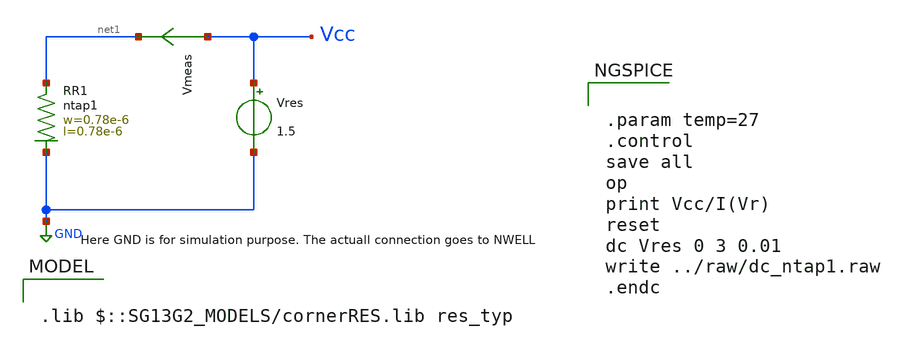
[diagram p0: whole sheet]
** sch_path: ihp-sg13g2/libs.tech/xschem/sg13g2_tests/dc_ntap1.sch
* Copyright 2023 IHP PDK Authors
**.subckt dc_ntap1
Vres Vcc GND 1.5
XR1 net1 GND ntap1 R=262.8 w=0.78e-6 l=0.78e-6
Vmeas Vcc net1 0
.save i(vmeas)
**** begin user architecture code

.lib $::SG13G2_MODELS/cornerRES.lib res_typ



.param temp=27
.control
save all
op
print Vcc/I(Vr)
reset
dc Vres 0 3 0.01
write ../raw/dc_ntap1.raw
.endc


**** end user architecture code
**.ends
.GLOBAL GND
.end
